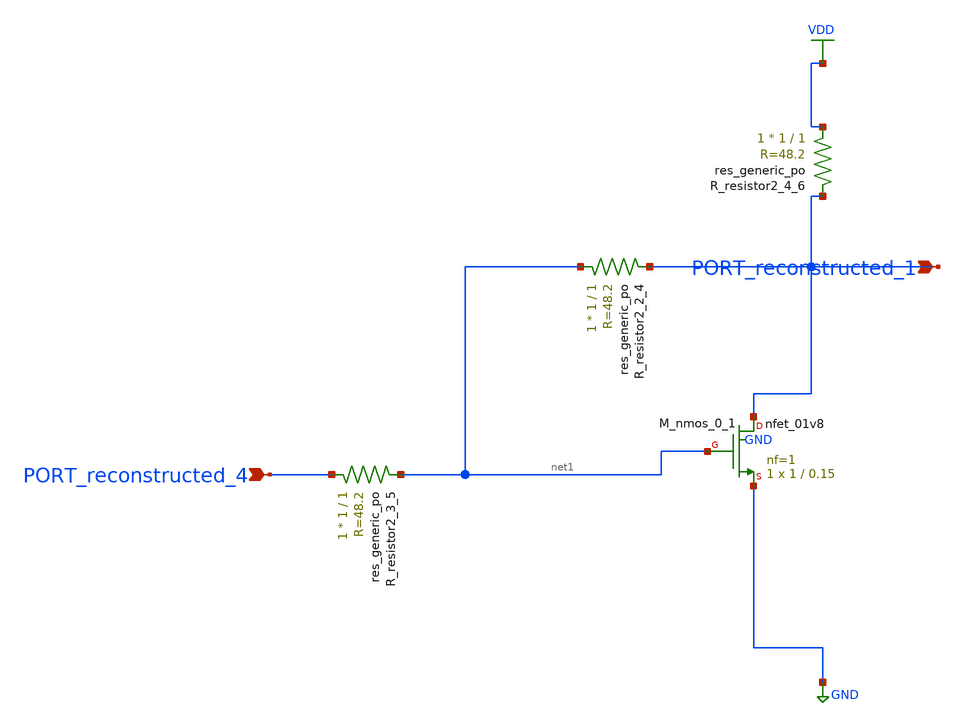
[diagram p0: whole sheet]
** sch_path: schematics/AMSNet/565.sch
**.subckt 565 PORT_reconstructed_1 PORT_reconstructed_4
*.ipin PORT_reconstructed_1
*.ipin PORT_reconstructed_4
XM_nmos_0_1 PORT_reconstructed_1 net1 GND GND sky130_fd_pr__nfet_01v8 L=0.15 W=1 nf=1 ad='int((1 + 1)/2) * 1 / 1 * 0.29'
+ as='int((1 + 2)/2) * 1 / 1 * 0.29' pd='2*int((1 + 1)/2) * (1 / 1 + 0.29)' ps='2*int((1 + 2)/2) * (1 / 1 + 0.29)'
+ nrd='0.29 / 1 ' nrs='0.29 / 1 ' sa=0 sb=0 sd=0 mult=1 m=1
XR_resistor2_2_4 net1 PORT_reconstructed_1 sky130_fd_pr__res_generic_po W=1 L=1 m=1
XR_resistor2_3_5 PORT_reconstructed_4 net1 sky130_fd_pr__res_generic_po W=1 L=1 m=1
XR_resistor2_4_6 VDD PORT_reconstructed_1 sky130_fd_pr__res_generic_po W=1 L=1 m=1
**.ends
.GLOBAL GND
.GLOBAL VDD
.end
